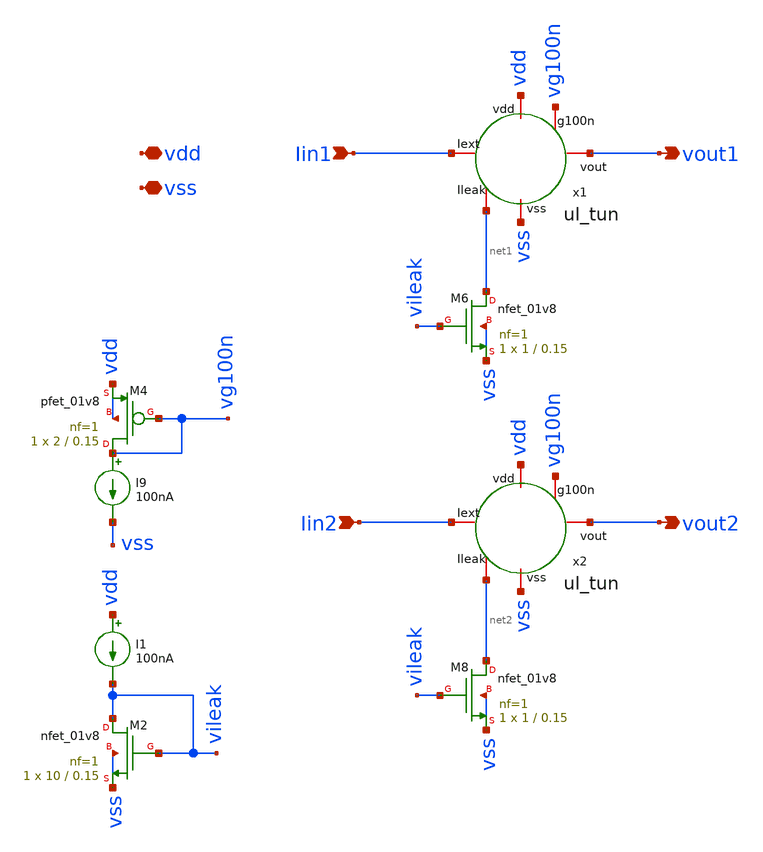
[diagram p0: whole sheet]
** sch_path: layer/layer_2_output.sch
**.subckt layer_2_output Iin1 Iin2 vout1 vout2 vdd vss
*.ipin Iin1
*.ipin Iin2
*.opin vout1
*.opin vout2
*.iopin vdd
*.iopin vss
x1 Iin1 vdd vg100n vout1 net1 vss ul_tun
XM6 net1 vileak vss vss sky130_fd_pr__nfet_01v8 L=0.15 W=1 nf=1 ad='int((nf+1)/2) * W/nf * 0.29' as='int((nf+2)/2) * W/nf * 0.29'
+ pd='2*int((nf+1)/2) * (W/nf + 0.29)' ps='2*int((nf+2)/2) * (W/nf + 0.29)' nrd='0.29 / W' nrs='0.29 / W'
+ sa=0 sb=0 sd=0 mult=1 m=1
x2 Iin2 vdd vg100n vout2 net2 vss ul_tun
XM8 net2 vileak vss vss sky130_fd_pr__nfet_01v8 L=0.15 W=1 nf=1 ad='int((nf+1)/2) * W/nf * 0.29' as='int((nf+2)/2) * W/nf * 0.29'
+ pd='2*int((nf+1)/2) * (W/nf + 0.29)' ps='2*int((nf+2)/2) * (W/nf + 0.29)' nrd='0.29 / W' nrs='0.29 / W'
+ sa=0 sb=0 sd=0 mult=1 m=1
I9 vg100n vss 100nA
XM4 vg100n vg100n vdd vdd sky130_fd_pr__pfet_01v8 L=0.15 W=2 nf=1 ad='int((nf+1)/2) * W/nf * 0.29' as='int((nf+2)/2) * W/nf * 0.29'
+ pd='2*int((nf+1)/2) * (W/nf + 0.29)' ps='2*int((nf+2)/2) * (W/nf + 0.29)' nrd='0.29 / W' nrs='0.29 / W'
+ sa=0 sb=0 sd=0 mult=1 m=1
XM2 vileak vileak vss vss sky130_fd_pr__nfet_01v8 L=0.15 W=10 nf=1 ad='int((nf+1)/2) * W/nf * 0.29' as='int((nf+2)/2) * W/nf * 0.29'
+ pd='2*int((nf+1)/2) * (W/nf + 0.29)' ps='2*int((nf+2)/2) * (W/nf + 0.29)' nrd='0.29 / W' nrs='0.29 / W'
+ sa=0 sb=0 sd=0 mult=1 m=1
I1 vdd vileak 100nA
**.ends

* expanding   symbol:  Neuron/ultralif/ul_tun.sym # of pins=6
** sym_path: Neuron/ultralif/ul_tun.sym
** sch_path: Neuron/ultralif/ul_tun.sch
.subckt ul_tun Iext vdd g100n vout Ileak vss
*.iopin Iext
*.iopin vout
*.iopin vss
*.iopin Ileak
*.iopin vdd
*.iopin g100n
XM1 Ileak Ileak net1 vdd sky130_fd_pr__pfet_01v8 L=10 W=1 nf=1 ad='int((nf+1)/2) * W/nf * 0.29' as='int((nf+2)/2) * W/nf * 0.29'
+ pd='2*int((nf+1)/2) * (W/nf + 0.29)' ps='2*int((nf+2)/2) * (W/nf + 0.29)' nrd='0.29 / W' nrs='0.29 / W'
+ sa=0 sb=0 sd=0 mult=1 m=1
XM2 Ileak net2 net1 vdd sky130_fd_pr__pfet_01v8 L=0.15 W=1.5 nf=1 ad='int((nf+1)/2) * W/nf * 0.29' as='int((nf+2)/2) * W/nf * 0.29'
+ pd='2*int((nf+1)/2) * (W/nf + 0.29)' ps='2*int((nf+2)/2) * (W/nf + 0.29)' nrd='0.29 / W' nrs='0.29 / W'
+ sa=0 sb=0 sd=0 mult=1 m=1
XM3 net2 net2 net1 vdd sky130_fd_pr__pfet_01v8 L=0.15 W=15 nf=1 ad='int((nf+1)/2) * W/nf * 0.29' as='int((nf+2)/2) * W/nf * 0.29'
+ pd='2*int((nf+1)/2) * (W/nf + 0.29)' ps='2*int((nf+2)/2) * (W/nf + 0.29)' nrd='0.29 / W' nrs='0.29 / W'
+ sa=0 sb=0 sd=0 mult=1 m=1
XM4 net2 Ileak vss vss sky130_fd_pr__nfet_01v8 L=4 W=1 nf=1 ad='int((1 + 1)/2) * 1 / 1 * 0.29' as='int((1 + 2)/2) * 1 / 1 * 0.29'
+ pd='2*int((1 + 1)/2) * (1 / 1 + 0.29)' ps='2*int((1 + 2)/2) * (1 / 1 + 0.29)' nrd='0.29 / 1 ' nrs='0.29 / 1 '
+ sa=0 sb=0 sd=0 mult=1 m=1
C1 net1 vss 1p m=1
XM5 vout_n Ileak vss vss sky130_fd_pr__nfet_01v8 L=0.15 W=1 nf=1 ad='int((1 + 1)/2) * 1 / 1 * 0.29' as='int((1 + 2)/2) * 1 / 1 * 0.29'
+ pd='2*int((1 + 1)/2) * (1 / 1 + 0.29)' ps='2*int((1 + 2)/2) * (1 / 1 + 0.29)' nrd='0.29 / 1 ' nrs='0.29 / 1 '
+ sa=0 sb=0 sd=0 mult=1 m=1
XM6 vout_n g100n vdd vdd sky130_fd_pr__pfet_01v8 L=0.15 W=2 nf=1 ad='int((nf+1)/2) * W/nf * 0.29' as='int((nf+2)/2) * W/nf * 0.29'
+ pd='2*int((nf+1)/2) * (W/nf + 0.29)' ps='2*int((nf+2)/2) * (W/nf + 0.29)' nrd='0.29 / W' nrs='0.29 / W'
+ sa=0 sb=0 sd=0 mult=1 m=1
XM7 vout vout_n vss vss sky130_fd_pr__nfet_01v8 L=0.15 W=1 nf=1 ad='int((1 + 1)/2) * 1 / 1 * 0.29' as='int((1 + 2)/2) * 1 / 1 * 0.29'
+ pd='2*int((1 + 1)/2) * (1 / 1 + 0.29)' ps='2*int((1 + 2)/2) * (1 / 1 + 0.29)' nrd='0.29 / 1 ' nrs='0.29 / 1 '
+ sa=0 sb=0 sd=0 mult=1 m=1
XM8 vout vout_n vdd vdd sky130_fd_pr__pfet_01v8 L=0.15 W=2 nf=1 ad='int((nf+1)/2) * W/nf * 0.29' as='int((nf+2)/2) * W/nf * 0.29'
+ pd='2*int((nf+1)/2) * (W/nf + 0.29)' ps='2*int((nf+2)/2) * (W/nf + 0.29)' nrd='0.29 / W' nrs='0.29 / W'
+ sa=0 sb=0 sd=0 mult=1 m=1
XM9 net3 Ileak Iext vdd sky130_fd_pr__pfet_01v8 L=0.15 W=4 nf=1 ad='int((nf+1)/2) * W/nf * 0.29' as='int((nf+2)/2) * W/nf * 0.29'
+ pd='2*int((nf+1)/2) * (W/nf + 0.29)' ps='2*int((nf+2)/2) * (W/nf + 0.29)' nrd='0.29 / W' nrs='0.29 / W'
+ sa=0 sb=0 sd=0 mult=1 m=1
vext net3 net1 0
**** begin user architecture code


.save i(vext) v(vout)


**** end user architecture code
.ends

.end
